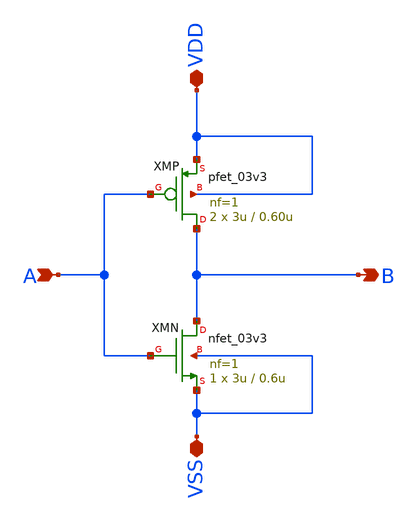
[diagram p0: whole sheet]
** sch_path: designs/sar_adc/digital/gate_inv_x1/xschem/gate_inv_x1.sch
**.subckt gate_inv_x1 B A VDD VSS
*.opin B
*.ipin A
*.iopin VDD
*.iopin VSS
XMN B A VSS VSS nfet_03v3 L=0.6u W=3u nf=1 ad='int((nf+1)/2) * W/nf * 0.18u' as='int((nf+2)/2) * W/nf * 0.18u'
+ pd='2*int((nf+1)/2) * (W/nf + 0.18u)' ps='2*int((nf+2)/2) * (W/nf + 0.18u)' nrd='0.18u / W' nrs='0.18u / W'
+ sa=0 sb=0 sd=0 m=1
XMP B A VDD VDD pfet_03v3 L=0.60u W=3u nf=1 ad='int((nf+1)/2) * W/nf * 0.18u' as='int((nf+2)/2) * W/nf * 0.18u'
+ pd='2*int((nf+1)/2) * (W/nf + 0.18u)' ps='2*int((nf+2)/2) * (W/nf + 0.18u)' nrd='0.18u / W' nrs='0.18u / W'
+ sa=0 sb=0 sd=0 m=2
**.ends
.end
